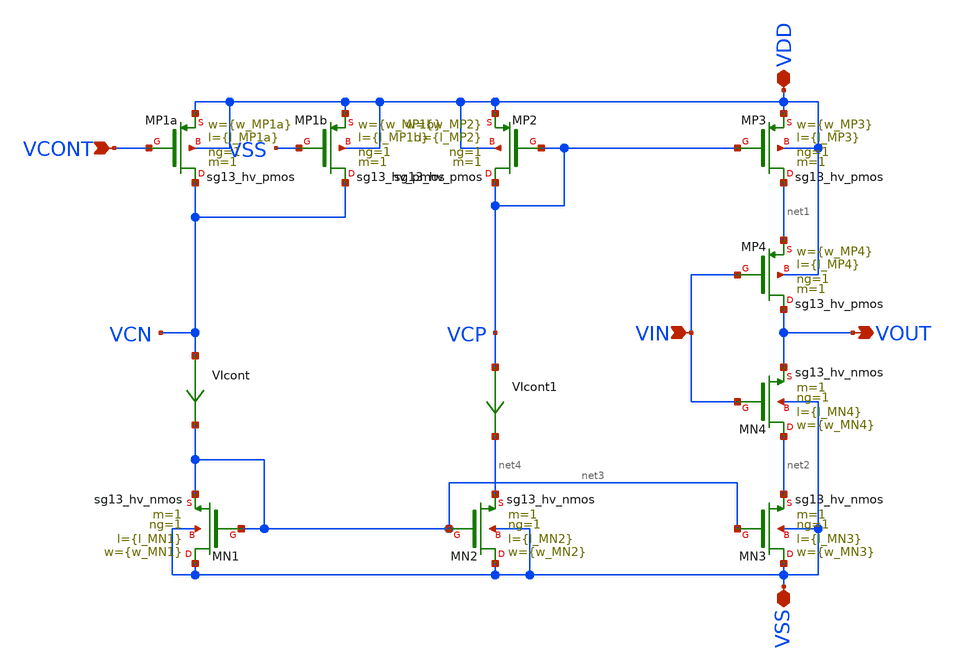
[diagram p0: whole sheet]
** sch_path: xschem/VCO/stage_IHP.sch
**.subckt stage_IHP VIN VOUT VDD VSS VCONT
*.ipin VIN
*.opin VOUT
*.iopin VDD
*.iopin VSS
*.ipin VCONT
XMN1 VSS net3 net3 VSS sg13_hv_nmos w={w_MN1} l={l_MN1} ng=1 m=1 mm_ok=1
XMN2 VSS net3 net4 VSS sg13_hv_nmos w={w_MN2} l={l_MN2} ng=1 m=1 mm_ok=1
XMN3 VSS net3 net2 VSS sg13_hv_nmos w={w_MN3} l={l_MN3} ng=1 m=1 mm_ok=1
XMP1a VCN VCONT VDD VDD sg13_hv_pmos w={w_MP1a} l={l_MP1a} ng=1 m=1 mm_ok=1
XMP2 VCP VCP VDD VDD sg13_hv_pmos w={w_MP2} l={l_MP2} ng=1 m=1 mm_ok=1
XMP3 net1 VCP VDD VDD sg13_hv_pmos w={w_MP3} l={l_MP3} ng=1 m=1 mm_ok=1
XMP4 VOUT VIN net1 VDD sg13_hv_pmos w={w_MP4} l={l_MP4} ng=1 m=1 mm_ok=1
XMN4 net2 VIN VOUT VSS sg13_hv_nmos w={w_MN4} l={l_MN4} ng=1 m=1 mm_ok=1
XMP1b VCN VSS VDD VDD sg13_hv_pmos w={w_MP1b} l={l_MP1b} ng=1 m=1 mm_ok=1
VIcont VCN net3 0
.save i(vicont)
VIcont1 VCP net4 0
.save i(vicont1)
**.ends
.end
